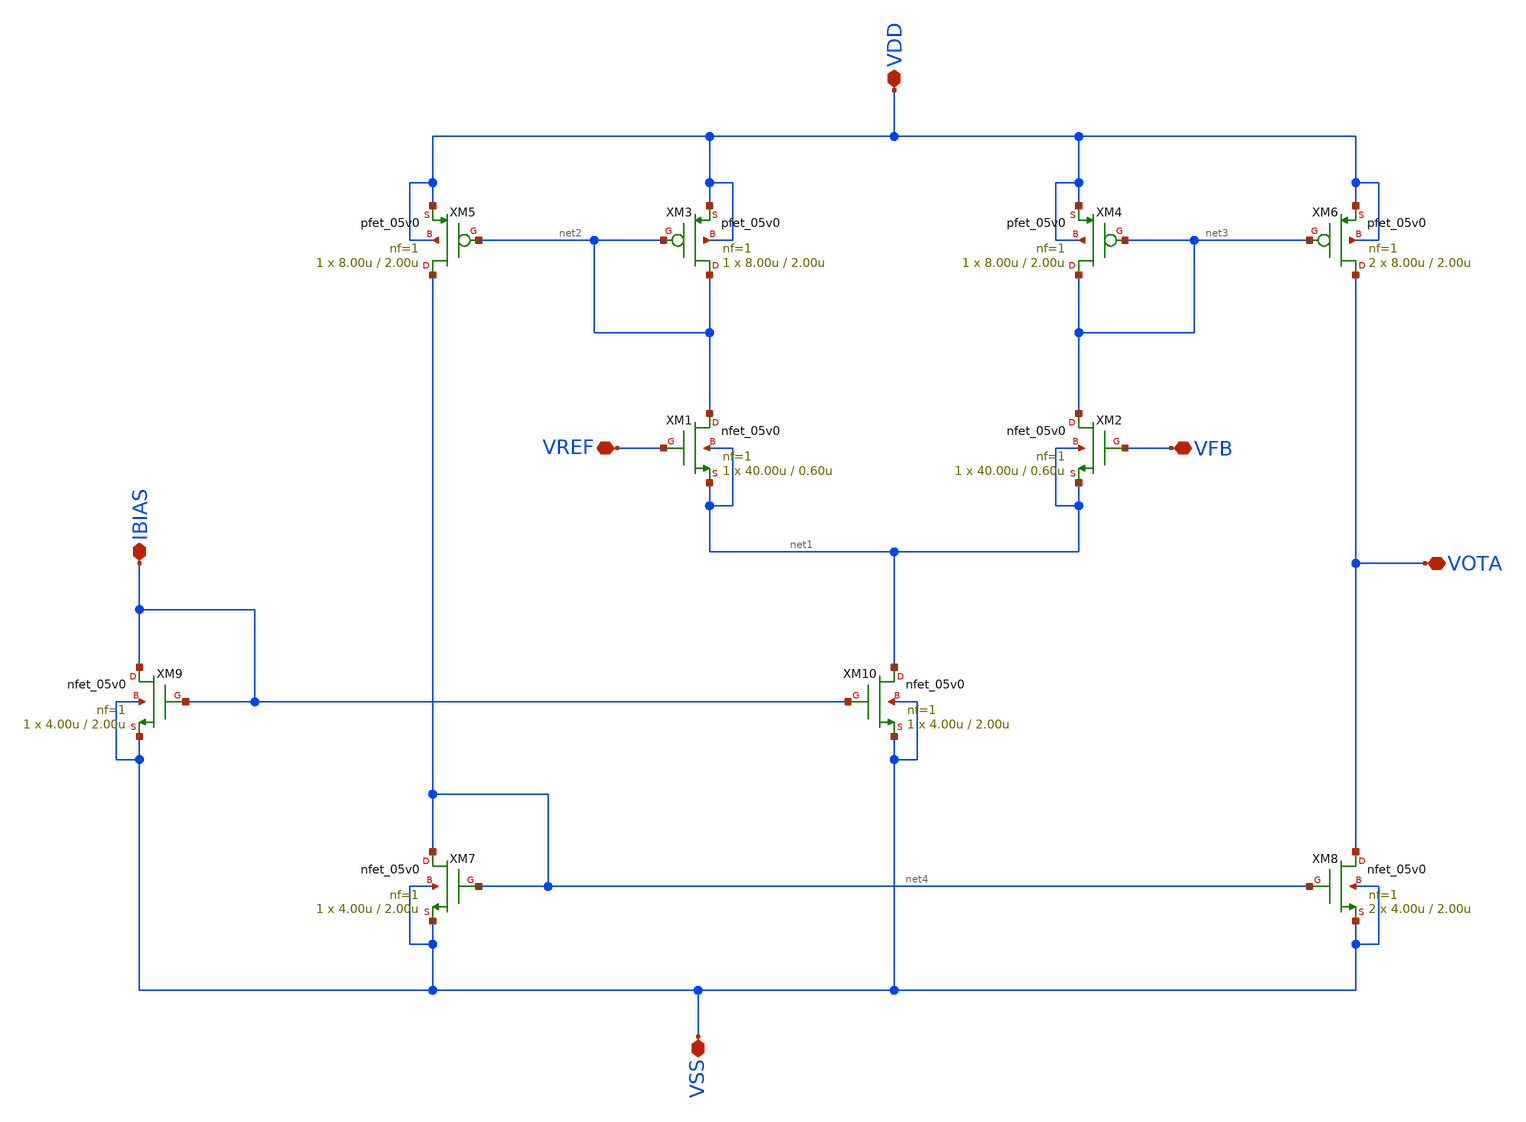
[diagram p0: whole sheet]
** sch_path: designs/libs/core_ldo/ldo/OTA.sch
**.subckt OTA VDD VSS VOTA VREF IBIAS VFB
*.iopin VDD
*.iopin VSS
*.iopin VOTA
*.iopin VREF
*.iopin IBIAS
*.iopin VFB
XM3 net2 net2 VDD VDD pfet_05v0 L=2.00u W=8.00u nf=1 ad='int((nf+1)/2) * W/nf * 0.18u' as='int((nf+2)/2) * W/nf * 0.18u'
+ pd='2*int((nf+1)/2) * (W/nf + 0.18u)' ps='2*int((nf+2)/2) * (W/nf + 0.18u)' nrd='0.18u / W' nrs='0.18u / W'
+ sa=0 sb=0 sd=0 m=1
XM4 net3 net3 VDD VDD pfet_05v0 L=2.00u W=8.00u nf=1 ad='int((nf+1)/2) * W/nf * 0.18u' as='int((nf+2)/2) * W/nf * 0.18u'
+ pd='2*int((nf+1)/2) * (W/nf + 0.18u)' ps='2*int((nf+2)/2) * (W/nf + 0.18u)' nrd='0.18u / W' nrs='0.18u / W'
+ sa=0 sb=0 sd=0 m=1
XM5 net4 net2 VDD VDD pfet_05v0 L=2.00u W=8.00u nf=1 ad='int((nf+1)/2) * W/nf * 0.18u' as='int((nf+2)/2) * W/nf * 0.18u'
+ pd='2*int((nf+1)/2) * (W/nf + 0.18u)' ps='2*int((nf+2)/2) * (W/nf + 0.18u)' nrd='0.18u / W' nrs='0.18u / W'
+ sa=0 sb=0 sd=0 m=1
XM6 VOTA net3 VDD VDD pfet_05v0 L=2.00u W=8.00u nf=1 ad='int((nf+1)/2) * W/nf * 0.18u' as='int((nf+2)/2) * W/nf * 0.18u'
+ pd='2*int((nf+1)/2) * (W/nf + 0.18u)' ps='2*int((nf+2)/2) * (W/nf + 0.18u)' nrd='0.18u / W' nrs='0.18u / W'
+ sa=0 sb=0 sd=0 m=2
XM9 IBIAS IBIAS VSS VSS nfet_05v0 L=2.00u W=4.00u nf=1 ad='int((nf+1)/2) * W/nf * 0.18u' as='int((nf+2)/2) * W/nf * 0.18u'
+ pd='2*int((nf+1)/2) * (W/nf + 0.18u)' ps='2*int((nf+2)/2) * (W/nf + 0.18u)' nrd='0.18u / W' nrs='0.18u / W'
+ sa=0 sb=0 sd=0 m=1
XM10 net1 IBIAS VSS VSS nfet_05v0 L=2.00u W=4.00u nf=1 ad='int((nf+1)/2) * W/nf * 0.18u' as='int((nf+2)/2) * W/nf * 0.18u'
+ pd='2*int((nf+1)/2) * (W/nf + 0.18u)' ps='2*int((nf+2)/2) * (W/nf + 0.18u)' nrd='0.18u / W' nrs='0.18u / W'
+ sa=0 sb=0 sd=0 m=1
XM7 net4 net4 VSS VSS nfet_05v0 L=2.00u W=4.00u nf=1 ad='int((nf+1)/2) * W/nf * 0.18u' as='int((nf+2)/2) * W/nf * 0.18u'
+ pd='2*int((nf+1)/2) * (W/nf + 0.18u)' ps='2*int((nf+2)/2) * (W/nf + 0.18u)' nrd='0.18u / W' nrs='0.18u / W'
+ sa=0 sb=0 sd=0 m=1
XM8 VOTA net4 VSS VSS nfet_05v0 L=2.00u W=4.00u nf=1 ad='int((nf+1)/2) * W/nf * 0.18u' as='int((nf+2)/2) * W/nf * 0.18u'
+ pd='2*int((nf+1)/2) * (W/nf + 0.18u)' ps='2*int((nf+2)/2) * (W/nf + 0.18u)' nrd='0.18u / W' nrs='0.18u / W'
+ sa=0 sb=0 sd=0 m=2
XM1 net2 VREF net1 net1 nfet_05v0 L=0.60u W=40.00u nf=1 ad='int((nf+1)/2) * W/nf * 0.18u' as='int((nf+2)/2) * W/nf * 0.18u'
+ pd='2*int((nf+1)/2) * (W/nf + 0.18u)' ps='2*int((nf+2)/2) * (W/nf + 0.18u)' nrd='0.18u / W' nrs='0.18u / W'
+ sa=0 sb=0 sd=0 m=1
XM2 net3 VFB net1 net1 nfet_05v0 L=0.60u W=40.00u nf=1 ad='int((nf+1)/2) * W/nf * 0.18u' as='int((nf+2)/2) * W/nf * 0.18u'
+ pd='2*int((nf+1)/2) * (W/nf + 0.18u)' ps='2*int((nf+2)/2) * (W/nf + 0.18u)' nrd='0.18u / W' nrs='0.18u / W'
+ sa=0 sb=0 sd=0 m=1
**.ends
.end
